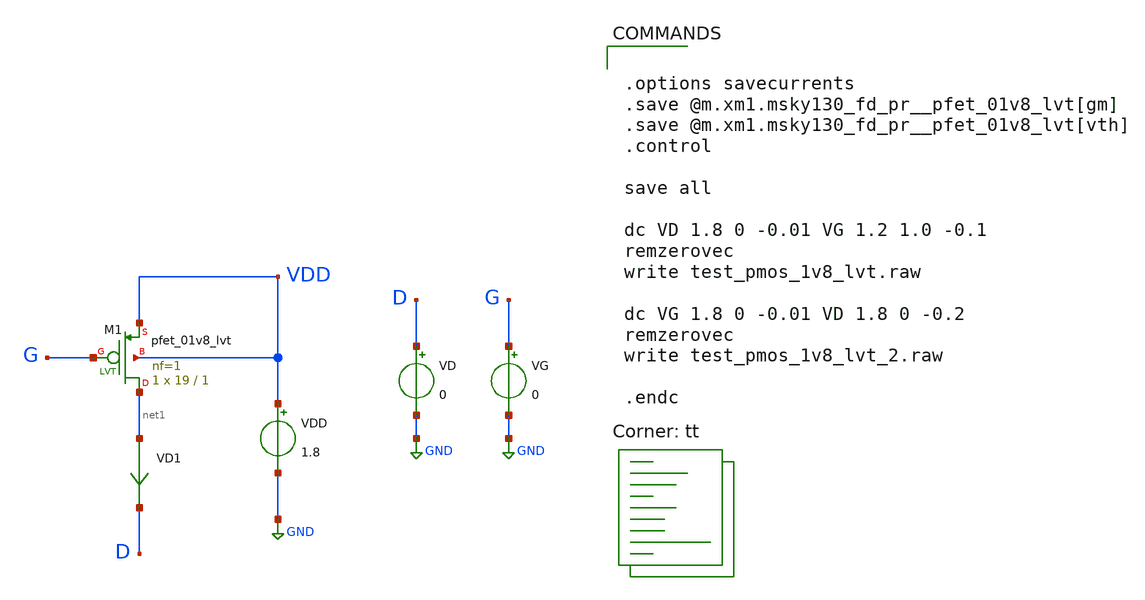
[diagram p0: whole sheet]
** sch_path: strongARM/test_pmos_1v8_lvt.sch
**.subckt test_pmos_1v8_lvt
VG G GND 0
VDD VDD GND 1.8
VD1 net1 D 0
.save i(vd1)
VD D GND 0
XM1 net1 G VDD VDD sky130_fd_pr__pfet_01v8_lvt L=1 W=19 nf=1 ad='int((nf+1)/2) * W/nf * 0.29' as='int((nf+2)/2) * W/nf * 0.29'
+ pd='2*int((nf+1)/2) * (W/nf + 0.29)' ps='2*int((nf+2)/2) * (W/nf + 0.29)' nrd='0.29 / W' nrs='0.29 / W'
+ sa=0 sb=0 sd=0 mult=1 m=1
**** begin user architecture code
.lib $::SKYWATER_MODELS/sky130.lib.spice tt


.options savecurrents
.save @m.xm1.msky130_fd_pr__pfet_01v8_lvt[gm]
.save @m.xm1.msky130_fd_pr__pfet_01v8_lvt[vth]
.control

save all

dc VD 1.8 0 -0.01 VG 1.2 1.0 -0.1
remzerovec
write test_pmos_1v8_lvt.raw

dc VG 1.8 0 -0.01 VD 1.8 0 -0.2
remzerovec
write test_pmos_1v8_lvt_2.raw

.endc


**** end user architecture code
**.ends
.GLOBAL GND
.end
